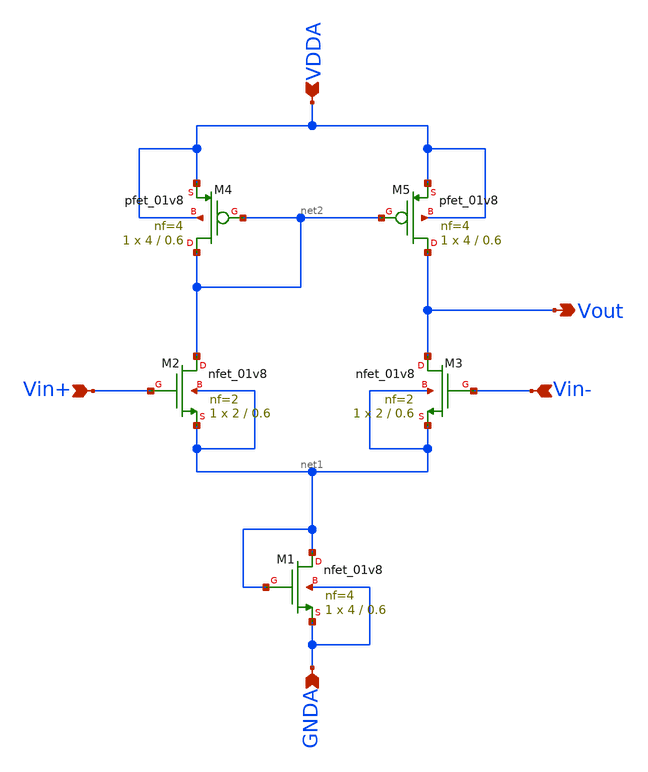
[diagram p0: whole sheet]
** sch_path: projects/bandgapref/xschem_ngspice/new_files/opamp_bandgap.sch
**.subckt opamp_bandgap Vin+ Vout Vin- GNDA VDDA
*.ipin Vin+
*.opin Vout
*.ipin Vin-
*.ipin GNDA
*.ipin VDDA
XM1 net1 net1 GNDA GNDA sky130_fd_pr__nfet_01v8 L=0.6 W=4 nf=4 ad='int((nf+1)/2) * W/nf * 0.29' as='int((nf+2)/2) * W/nf * 0.29'
+ pd='2*int((nf+1)/2) * (W/nf + 0.29)' ps='2*int((nf+2)/2) * (W/nf + 0.29)' nrd='0.29 / W' nrs='0.29 / W'
+ sa=0 sb=0 sd=0 mult=1 m=1
XM2 net2 Vin+ net1 net1 sky130_fd_pr__nfet_01v8 L=0.6 W=2 nf=2 ad='int((nf+1)/2) * W/nf * 0.29' as='int((nf+2)/2) * W/nf * 0.29'
+ pd='2*int((nf+1)/2) * (W/nf + 0.29)' ps='2*int((nf+2)/2) * (W/nf + 0.29)' nrd='0.29 / W' nrs='0.29 / W'
+ sa=0 sb=0 sd=0 mult=1 m=1
XM3 Vout Vin- net1 net1 sky130_fd_pr__nfet_01v8 L=0.6 W=2 nf=2 ad='int((nf+1)/2) * W/nf * 0.29' as='int((nf+2)/2) * W/nf * 0.29'
+ pd='2*int((nf+1)/2) * (W/nf + 0.29)' ps='2*int((nf+2)/2) * (W/nf + 0.29)' nrd='0.29 / W' nrs='0.29 / W'
+ sa=0 sb=0 sd=0 mult=1 m=1
XM4 net2 net2 VDDA VDDA sky130_fd_pr__pfet_01v8 L=0.6 W=4 nf=4 ad='int((nf+1)/2) * W/nf * 0.29' as='int((nf+2)/2) * W/nf * 0.29'
+ pd='2*int((nf+1)/2) * (W/nf + 0.29)' ps='2*int((nf+2)/2) * (W/nf + 0.29)' nrd='0.29 / W' nrs='0.29 / W'
+ sa=0 sb=0 sd=0 mult=1 m=1
XM5 Vout net2 VDDA VDDA sky130_fd_pr__pfet_01v8 L=0.6 W=4 nf=4 ad='int((nf+1)/2) * W/nf * 0.29' as='int((nf+2)/2) * W/nf * 0.29'
+ pd='2*int((nf+1)/2) * (W/nf + 0.29)' ps='2*int((nf+2)/2) * (W/nf + 0.29)' nrd='0.29 / W' nrs='0.29 / W'
+ sa=0 sb=0 sd=0 mult=1 m=1
**.ends
.end
